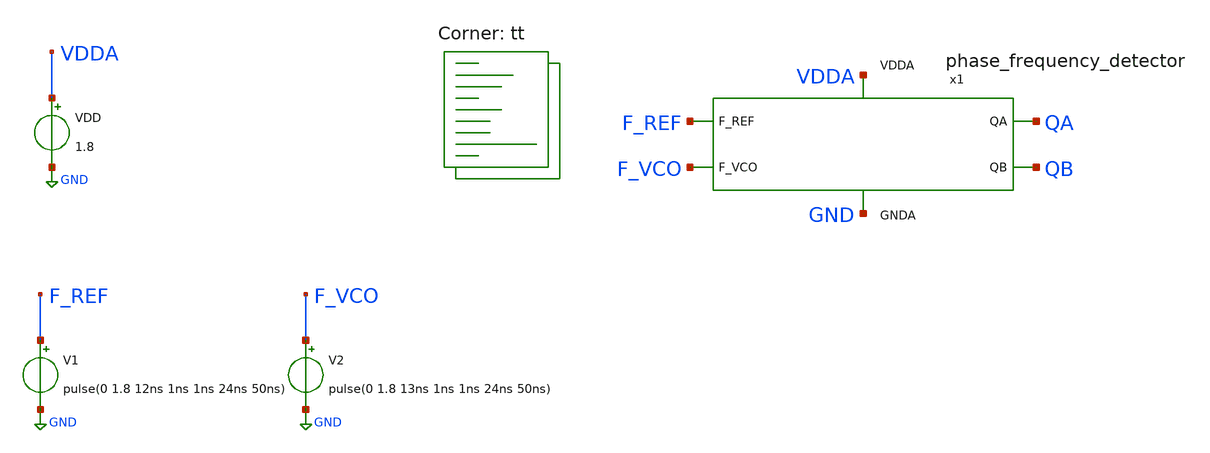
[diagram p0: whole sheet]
** sch_path: projects/pll/pfd/xschem_ngspice/tb_phase_frequency_detector.sch
**.subckt tb_phase_frequency_detector
V1 F_REF GND pulse(0 1.8 12ns 1ns 1ns 24ns 50ns)
V2 F_VCO GND pulse(0 1.8 13ns 1ns 1ns 24ns 50ns)
VDD VDDA GND 1.8
x1 F_REF F_VCO VDDA QA QB GND phase_frequency_detector
**** begin user architecture code
.lib $::SKYWATER_MODELS/sky130.lib.spice tt



.include /foss/pdks/sky130A/libs.ref/sky130_fd_sc_hd/spice/sky130_fd_sc_hd.spice


.option wnflag=1
.option method=gear trtol=1

* .ic v(osc)=0
* .temp = 75

.save v(x1.reset)
.save v(x1.qb_b)
.save v(x1.qa_b)
.save v(x1.f_b)
.save v(x1.f)
.save v(x1.e_b)
.save v(x1.e)
.save v(x1.before_reset)
.save v(qb)
.save v(qa)
.save v(f_vco)
.save v(f_ref)
.save v(f_vco)


.control

  tran 1ns 1us
  remzerovec
  write tb_phase_frequency_detector.raw
  * write tb_phase_frequency_detector_2.raw
  linearize v(qa) v(qb)
  wrdata /foss/designs/my_design/projects/pll/pfd/xschem_ngspice/tb_phase_frequency_detector_QA.txt
+ v(qa)
  wrdata /foss/designs/my_design/projects/pll/pfd/xschem_ngspice/tb_phase_frequency_detector_QB.txt
+ v(qb)

  set appendwrite

.endc






**** end user architecture code
**.ends

* expanding   symbol:
*+  /foss/designs/my_design/projects/pll/pfd/xschem_ngspice/phase_frequency_detector.sym # of pins=6
** sym_path: projects/pll/pfd/xschem_ngspice/phase_frequency_detector.sym
** sch_path: projects/pll/pfd/xschem_ngspice/phase_frequency_detector.sch
.subckt phase_frequency_detector F_REF F_VCO VDDA QA QB GNDA
*.ipin F_REF
*.opin QA
*.ipin F_VCO
*.opin QB
*.ipin VDDA
*.ipin GNDA
x1 F_REF QA GNDA GNDA VDDA VDDA QA_b sky130_fd_sc_hd__nor2_1
x2 E QA_b GNDA GNDA VDDA VDDA QA sky130_fd_sc_hd__nor2_1
x3 QA_b E_b GNDA GNDA VDDA VDDA E sky130_fd_sc_hd__nor2_1
x4 Reset E GNDA GNDA VDDA VDDA E_b sky130_fd_sc_hd__nor2_1
x5 F_VCO QB GNDA GNDA VDDA VDDA QB_b sky130_fd_sc_hd__nor2_1
x6 F QB_b GNDA GNDA VDDA VDDA QB sky130_fd_sc_hd__nor2_1
x7 QB_b F_b GNDA GNDA VDDA VDDA F sky130_fd_sc_hd__nor2_1
x8 Reset F GNDA GNDA VDDA VDDA F_b sky130_fd_sc_hd__nor2_1
x9 QB QA GNDA GNDA VDDA VDDA before_Reset sky130_fd_sc_hd__nand2_1
x10 before_Reset GNDA GNDA VDDA VDDA net1 sky130_fd_sc_hd__inv_1
x11 net1 GNDA GNDA VDDA VDDA net2 sky130_fd_sc_hd__inv_1
x12 net2 GNDA GNDA VDDA VDDA net3 sky130_fd_sc_hd__inv_1
x13 net3 GNDA GNDA VDDA VDDA net4 sky130_fd_sc_hd__inv_1
x14 net4 GNDA GNDA VDDA VDDA Reset sky130_fd_sc_hd__inv_1
.ends

.GLOBAL GND
.end
